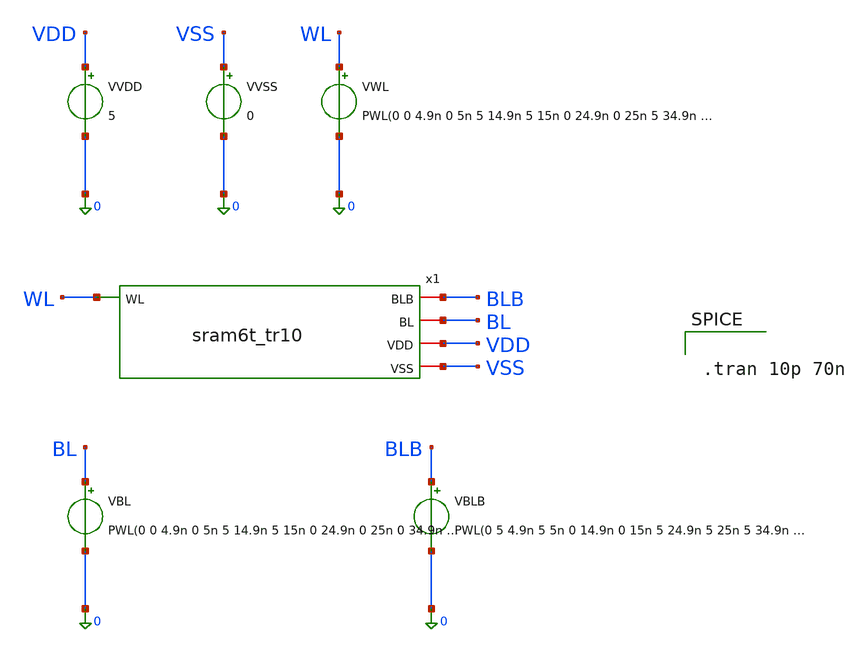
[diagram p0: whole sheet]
** sch_path: cell/tb_write.sch
**.subckt tb_write
VVDD VDD 0 5
VWL WL 0 PWL(0 0 4.9n 0 5n 5 14.9n 5 15n 0 24.9n 0 25n 5 34.9n 5 35n 0 44.9n 0 45n 5 54.9n 5 55n 0
+ 70n 0)
VBL BL 0 PWL(0 0 4.9n 0 5n 5 14.9n 5 15n 0 24.9n 0 25n 0 34.9n 0 35n 0 44.9n 0 45n 5 54.9n 5 55n 0
+ 70n 0)
VBLB BLB 0 PWL(0 5 4.9n 5 5n 0 14.9n 0 15n 5 24.9n 5 25n 5 34.9n 5 35n 5 44.9n 5 45n 0 54.9n 0 55n 5
+ 70n 5)
VVSS VSS 0 0
x1 BL BLB WL VDD VSS sram6t_tr10
**** begin user architecture code
 .include $::LIB/ip62_models


.tran 10p 70n


**** end user architecture code
**.ends
.end
